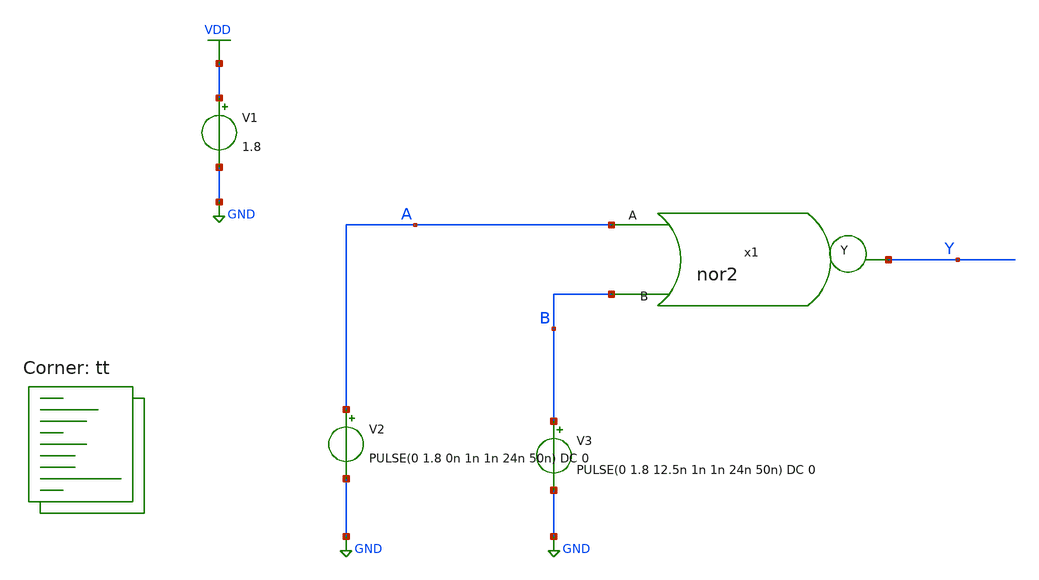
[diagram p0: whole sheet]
** sch_path: eng331lab_final/eng331lab_xschem/tb_nor2.sch
**.subckt tb_nor2
x1 A B Y nor2
V1 VDD GND 1.8
V2 A GND PULSE(0 1.8 0n 1n 1n 24n 50n) DC 0
V3 B GND PULSE(0 1.8 12.5n 1n 1n 24n 50n) DC 0
**** begin user architecture code

.control
  save all
  tran 10n 400n
  write tb_nor2.raw
  set appendwrite
.endc


.lib $::SKYWATER_MODELS/sky130.lib.spice tt
**** end user architecture code
**.ends

* expanding   symbol:  eng331lab_xschem/nor2.sym # of pins=3
** sym_path: eng331lab_final/eng331lab_xschem/nor2.sym
** sch_path: eng331lab_final/eng331lab_xschem/nor2.sch
.subckt nor2 A B Y
*.ipin A
*.ipin B
*.opin Y
XM1 net1 A VDD VDD sky130_fd_pr__pfet_01v8 L=0.15 W=1.6 nf=1 ad='int((1 + 1)/2) * 1.6 / 1 * 0.29' as='int((1 + 2)/2) * 1.6 / 1 * 0.29'
+ pd='2*int((1 + 1)/2) * (1.6 / 1 + 0.29)' ps='2*int((1 + 2)/2) * (1.6 / 1 + 0.29)' nrd='0.29 / 1.6 ' nrs='0.29 / 1.6 '
+ sa=0 sb=0 sd=0 mult=1 m=1
XM2 Y B net1 VDD sky130_fd_pr__pfet_01v8 L=0.15 W=1.6 nf=1 ad='int((1 + 1)/2) * 1.6 / 1 * 0.29' as='int((1 + 2)/2) * 1.6 / 1 * 0.29'
+ pd='2*int((1 + 1)/2) * (1.6 / 1 + 0.29)' ps='2*int((1 + 2)/2) * (1.6 / 1 + 0.29)' nrd='0.29 / 1.6 ' nrs='0.29 / 1.6 '
+ sa=0 sb=0 sd=0 mult=1 m=1
XM3 Y A GND GND sky130_fd_pr__nfet_01v8 L=0.15 W=0.5 nf=1 ad='int((1 + 1)/2) * 0.5 / 1 * 0.29' as='int((1 + 2)/2) * 0.5 / 1 * 0.29'
+ pd='2*int((1 + 1)/2) * (0.5 / 1 + 0.29)' ps='2*int((1 + 2)/2) * (0.5 / 1 + 0.29)' nrd='0.29 / 0.5 ' nrs='0.29 / 0.5 '
+ sa=0 sb=0 sd=0 mult=1 m=1
XM4 Y B GND GND sky130_fd_pr__nfet_01v8 L=0.15 W=0.5 nf=1 ad='int((1 + 1)/2) * 0.5 / 1 * 0.29' as='int((1 + 2)/2) * 0.5 / 1 * 0.29'
+ pd='2*int((1 + 1)/2) * (0.5 / 1 + 0.29)' ps='2*int((1 + 2)/2) * (0.5 / 1 + 0.29)' nrd='0.29 / 0.5 ' nrs='0.29 / 0.5 '
+ sa=0 sb=0 sd=0 mult=1 m=1
.ends

.GLOBAL VDD
.GLOBAL GND
.end
